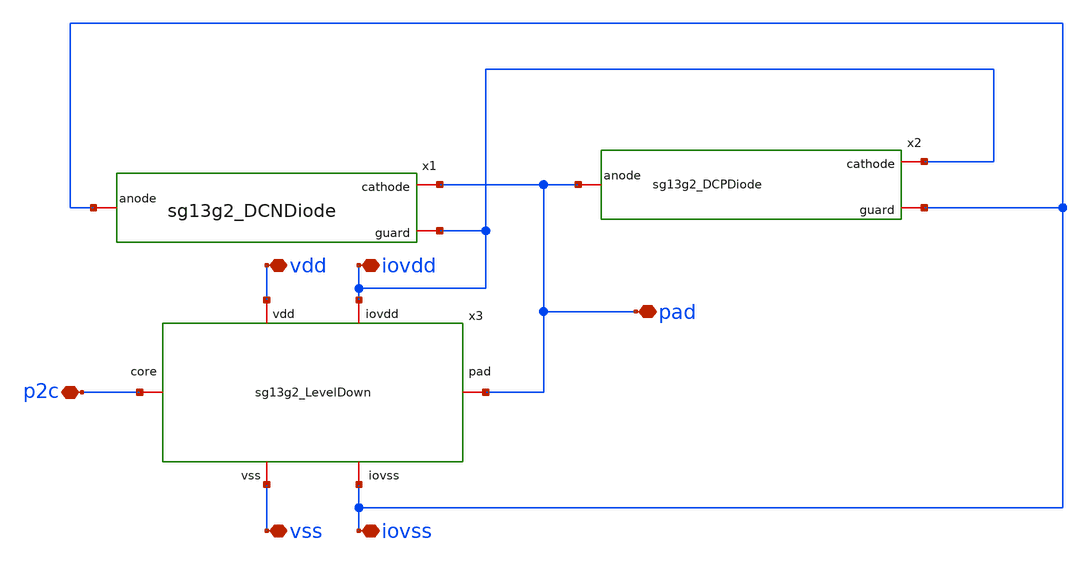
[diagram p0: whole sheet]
** sch_path: CDR4176-main/schematic/xschem/project_io/sg13g2_IOPadIn/sg13g2_IOPadIn.sch
**.subckt sg13g2_IOPadIn iovdd vdd vss iovss p2c pad
*.iopin iovdd
*.iopin vdd
*.iopin vss
*.iopin iovss
*.iopin p2c
*.iopin pad
x1 pad iovss iovdd sg13g2_DCNDiode
x2 iovdd pad iovss sg13g2_DCPDiode
x3 vdd iovdd p2c pad iovss vss sg13g2_LevelDown
**.ends
.end
